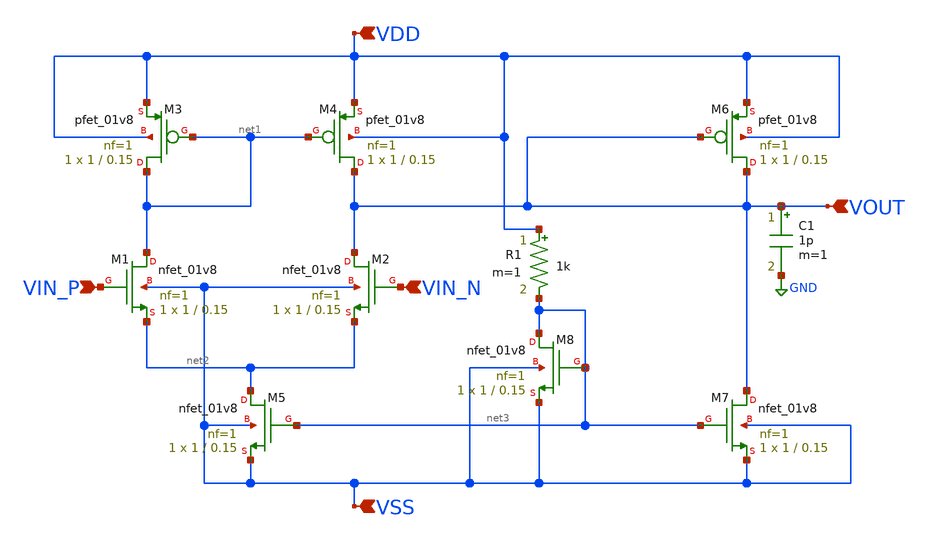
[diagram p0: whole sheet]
** sch_path: analog/symbols/bootcamp_opamp.sch
**.subckt bootcamp_opamp VIN_P VIN_N VDD VOUT VSS
*.ipin VIN_P
*.ipin VIN_N
*.ipin VDD
*.ipin VOUT
*.ipin VSS
XM1 net1 VIN_P net2 VSS sky130_fd_pr__nfet_01v8 L=0.15 W=1 nf=1 ad='int((nf+1)/2) * W/nf * 0.29' as='int((nf+2)/2) * W/nf * 0.29'
+ pd='2*int((nf+1)/2) * (W/nf + 0.29)' ps='2*int((nf+2)/2) * (W/nf + 0.29)' nrd='0.29 / W' nrs='0.29 / W'
+ sa=0 sb=0 sd=0 mult=1 m=1
XM2 VOUT VIN_N net2 VSS sky130_fd_pr__nfet_01v8 L=0.15 W=1 nf=1 ad='int((nf+1)/2) * W/nf * 0.29' as='int((nf+2)/2) * W/nf * 0.29'
+ pd='2*int((nf+1)/2) * (W/nf + 0.29)' ps='2*int((nf+2)/2) * (W/nf + 0.29)' nrd='0.29 / W' nrs='0.29 / W'
+ sa=0 sb=0 sd=0 mult=1 m=1
XM3 net1 net1 VDD VDD sky130_fd_pr__pfet_01v8 L=0.15 W=1 nf=1 ad='int((nf+1)/2) * W/nf * 0.29' as='int((nf+2)/2) * W/nf * 0.29'
+ pd='2*int((nf+1)/2) * (W/nf + 0.29)' ps='2*int((nf+2)/2) * (W/nf + 0.29)' nrd='0.29 / W' nrs='0.29 / W'
+ sa=0 sb=0 sd=0 mult=1 m=1
XM4 VOUT net1 VDD VDD sky130_fd_pr__pfet_01v8 L=0.15 W=1 nf=1 ad='int((nf+1)/2) * W/nf * 0.29' as='int((nf+2)/2) * W/nf * 0.29'
+ pd='2*int((nf+1)/2) * (W/nf + 0.29)' ps='2*int((nf+2)/2) * (W/nf + 0.29)' nrd='0.29 / W' nrs='0.29 / W'
+ sa=0 sb=0 sd=0 mult=1 m=1
XM5 net2 net3 VSS VSS sky130_fd_pr__nfet_01v8 L=0.15 W=1 nf=1 ad='int((nf+1)/2) * W/nf * 0.29' as='int((nf+2)/2) * W/nf * 0.29'
+ pd='2*int((nf+1)/2) * (W/nf + 0.29)' ps='2*int((nf+2)/2) * (W/nf + 0.29)' nrd='0.29 / W' nrs='0.29 / W'
+ sa=0 sb=0 sd=0 mult=1 m=1
XM6 VOUT VOUT VDD VDD sky130_fd_pr__pfet_01v8 L=0.15 W=1 nf=1 ad='int((nf+1)/2) * W/nf * 0.29' as='int((nf+2)/2) * W/nf * 0.29'
+ pd='2*int((nf+1)/2) * (W/nf + 0.29)' ps='2*int((nf+2)/2) * (W/nf + 0.29)' nrd='0.29 / W' nrs='0.29 / W'
+ sa=0 sb=0 sd=0 mult=1 m=1
XM7 VOUT net3 VSS VSS sky130_fd_pr__nfet_01v8 L=0.15 W=1 nf=1 ad='int((nf+1)/2) * W/nf * 0.29' as='int((nf+2)/2) * W/nf * 0.29'
+ pd='2*int((nf+1)/2) * (W/nf + 0.29)' ps='2*int((nf+2)/2) * (W/nf + 0.29)' nrd='0.29 / W' nrs='0.29 / W'
+ sa=0 sb=0 sd=0 mult=1 m=1
C1 VOUT GND 1p m=1
XM8 net3 net3 VSS VSS sky130_fd_pr__nfet_01v8 L=0.15 W=1 nf=1 ad='int((nf+1)/2) * W/nf * 0.29' as='int((nf+2)/2) * W/nf * 0.29'
+ pd='2*int((nf+1)/2) * (W/nf + 0.29)' ps='2*int((nf+2)/2) * (W/nf + 0.29)' nrd='0.29 / W' nrs='0.29 / W'
+ sa=0 sb=0 sd=0 mult=1 m=1
R1 VDD net3 1k m=1
**.ends
.GLOBAL GND
.end
